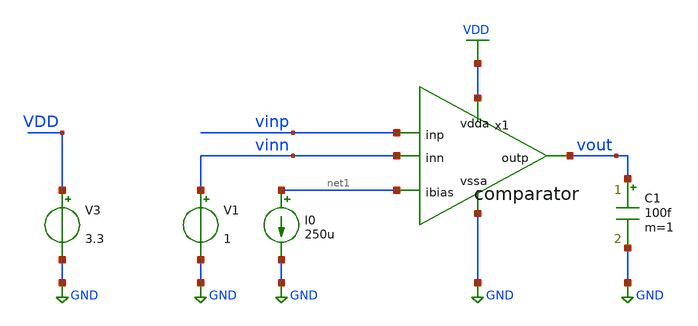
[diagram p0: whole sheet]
** sch_path: xschem/tb_comp_tran.sch
**.subckt tb_comp_tran
I0 net1 GND 250u
C1 vout GND 100f m=1
V1 vinn GND 1
V3 VDD GND 3.3
x1 VDD net1 vinp vinn vout GND comparator
**** begin user architecture code



.lib /home/ttuser/pdk/sky130A/libs.tech/ngspice/sky130.lib.spice tt

*.option temp=27
vinsource vinp 0 pulse(0 3.3 0 100NS 100NS 1u 2u 1)

.control
  tran 0.1ns 0.2us
  plot v(vout) v(vinp) v(vinn)
.endc

.save all



**** end user architecture code
**.ends
.GLOBAL GND
.GLOBAL VDD
.end
